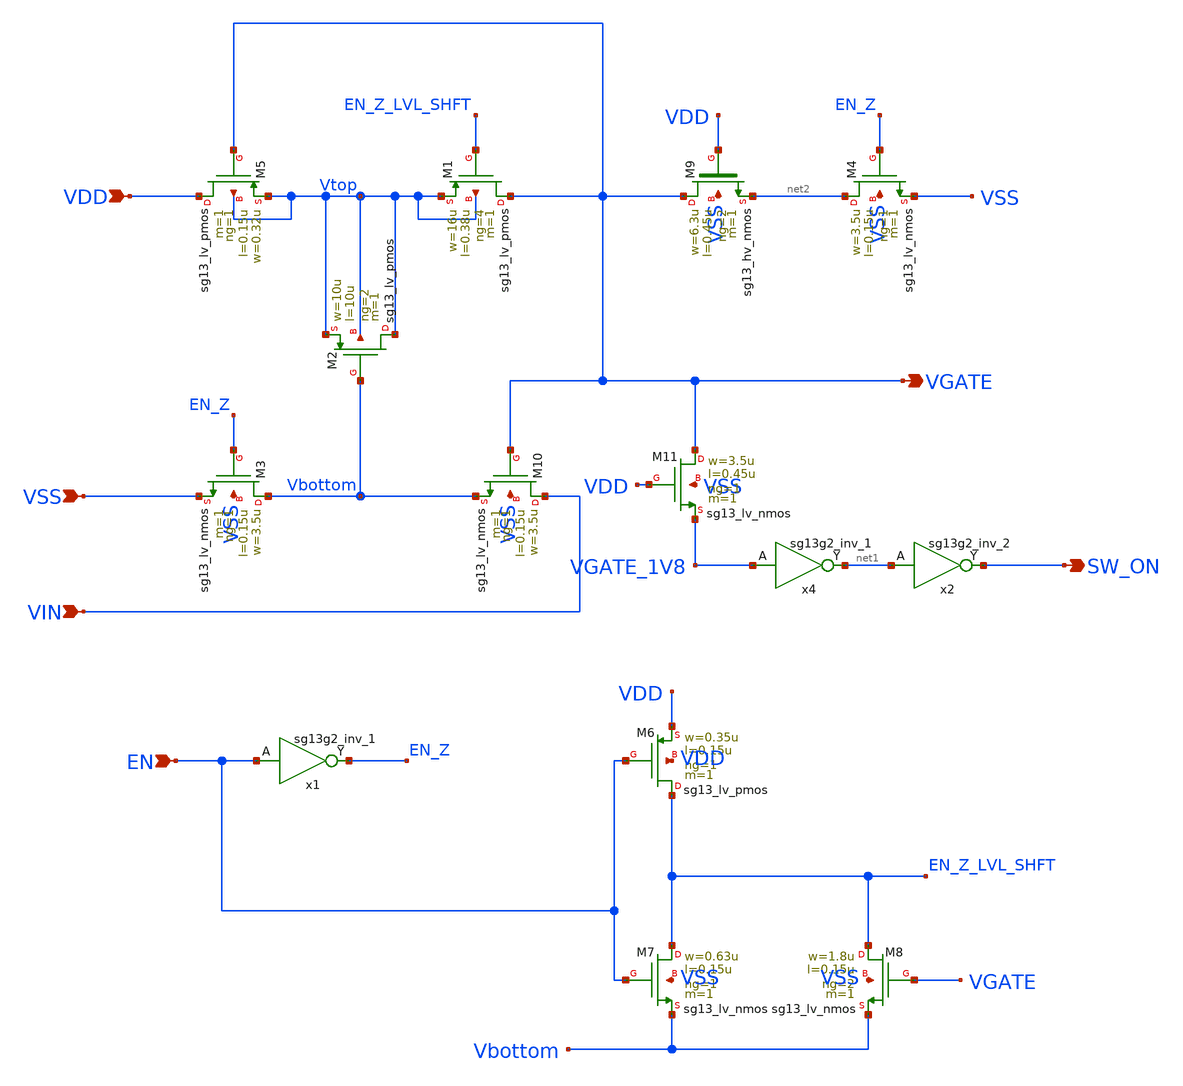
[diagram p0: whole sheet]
** sch_path: schematic/bootstrap/bootstrap.sch
* IHP-GmbH/IHP-Open-PDK/ihp-sg13g2/libs.tech/xschem/sg13g2_stdcells/sg13g2_inv_2.sch:
* Copyright 2023 IHP PDK Authors
* Licensed under the Apache License, Version 2.0 (the "License");
**.subckt bootstrap VDD VSS VIN EN VGATE SW_ON
*.ipin VDD
*.ipin VSS
*.ipin VIN
*.ipin EN
*.opin VGATE
*.opin SW_ON
XM5 VDD VGATE Vtop Vtop sg13_lv_pmos w=0.32u l=0.15u ng=1 m=1 mm_ok=1
XM1 VGATE EN_Z_LVL_SHFT Vtop Vtop sg13_lv_pmos w=16u l=0.38u ng=4 m=1 mm_ok=1
XM2 Vtop Vbottom Vtop Vtop sg13_lv_pmos w=10u l=10u ng=2 m=1 mm_ok=1
XM6 EN_Z_LVL_SHFT EN VDD VDD sg13_lv_pmos w=0.35u l=0.15u ng=1 m=1 mm_ok=1
XM7 EN_Z_LVL_SHFT EN Vbottom VSS sg13_lv_nmos w=0.63u l=0.15u ng=1 m=1 mm_ok=1
XM8 EN_Z_LVL_SHFT VGATE Vbottom VSS sg13_lv_nmos w=1.8u l=0.15u ng=2 m=1 mm_ok=1
XM3 Vbottom EN_Z VSS VSS sg13_lv_nmos w=3.5u l=0.15u ng=1 m=1 mm_ok=1
XM10 VIN VGATE Vbottom VSS sg13_lv_nmos w=3.5u l=0.15u ng=1 m=1 mm_ok=1
XM4 net2 EN_Z VSS VSS sg13_lv_nmos w=3.5u l=0.15u ng=1 m=1 mm_ok=1
XM11 VGATE VDD VGATE_1V8 VSS sg13_lv_nmos w=3.5u l=0.45u ng=1 m=1 mm_ok=1
XM9 VGATE VDD net2 VSS sg13_hv_nmos w=6.3u l=0.45u ng=2 m=1 mm_ok=1
x2 SW_ON net1 VDD VSS sg13g2_inv_2
x4 net1 VGATE_1V8 VDD VSS sg13g2_inv_1
x1 EN_Z EN VDD VSS sg13g2_inv_1
**.ends

* expanding   symbol:  sg13g2_stdcells/sg13g2_inv_2.sym # of pins=2
** sym_path: sg13g2_stdcells/sg13g2_inv_2.sym
** sch_path: sg13g2_stdcells/sg13g2_inv_2.sch
.subckt sg13g2_inv_2 Y A VDD VSS
*.opin Y
*.ipin A
*.iopin VDD
*.iopin VSS
XM1 Y A VSS VSS sg13_lv_nmos w=1.48u l=130.00n ng=2 m=1 mm_ok=1
XM2 Y A VDD VDD sg13_lv_pmos w=2.24u l=130.00n ng=2 m=1 mm_ok=1
.ends


* expanding   symbol:  sg13g2_stdcells/sg13g2_inv_1.sym # of pins=2
** sym_path: sg13g2_stdcells/sg13g2_inv_1.sym
** sch_path: sg13g2_stdcells/sg13g2_inv_1.sch
.subckt sg13g2_inv_1 Y A VDD VSS
*.opin Y
*.ipin A
*.iopin VDD
*.iopin VSS
XM1 Y A VSS VSS sg13_lv_nmos w=740.00n l=130.00n ng=1 m=1 mm_ok=1
XM2 Y A VDD VDD sg13_lv_pmos w=1.12u l=130.00n ng=1 m=1 mm_ok=1
.ends

.end
